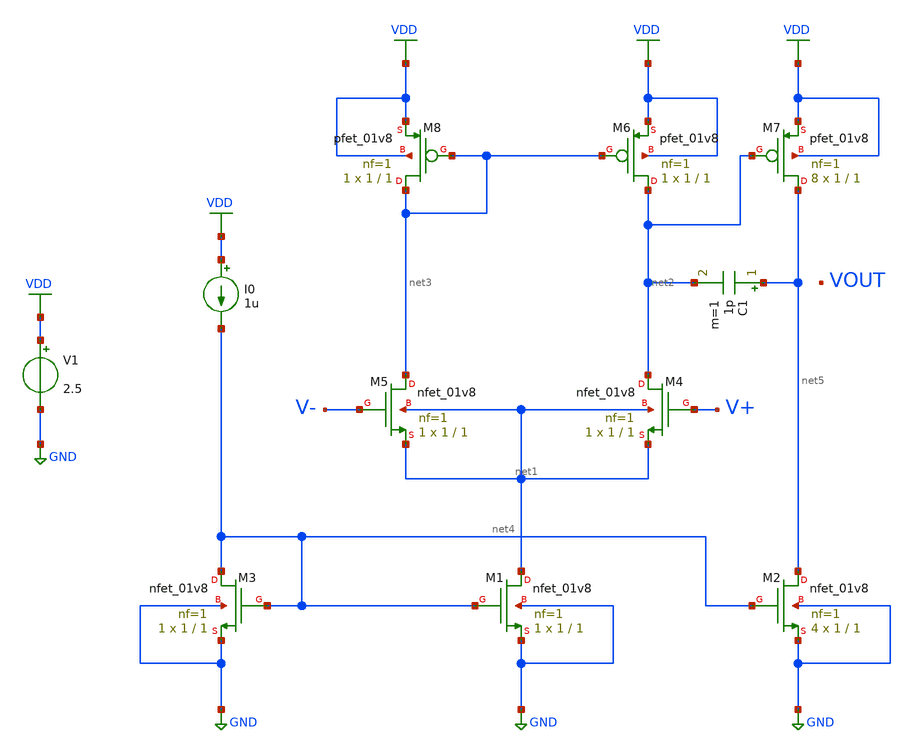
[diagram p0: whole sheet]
** sch_path: XSCHEM_SCHEMATICS/TEST_OPAMP_1/OPAMP_01.sch
**.subckt OPAMP_01
XM1 net1 net4 GND GND sky130_fd_pr__nfet_01v8 L=1 W=1 nf=1 ad='int((nf+1)/2) * W/nf * 0.29' as='int((nf+2)/2) * W/nf * 0.29'
+ pd='2*int((nf+1)/2) * (W/nf + 0.29)' ps='2*int((nf+2)/2) * (W/nf + 0.29)' nrd='0.29 / W' nrs='0.29 / W'
+ sa=0 sb=0 sd=0 mult=1 m=1
XM2 net5 net4 GND GND sky130_fd_pr__nfet_01v8 L=1 W=1 nf=1 ad='int((nf+1)/2) * W/nf * 0.29' as='int((nf+2)/2) * W/nf * 0.29'
+ pd='2*int((nf+1)/2) * (W/nf + 0.29)' ps='2*int((nf+2)/2) * (W/nf + 0.29)' nrd='0.29 / W' nrs='0.29 / W'
+ sa=0 sb=0 sd=0 mult=4 m=4
XM3 net4 net4 GND GND sky130_fd_pr__nfet_01v8 L=1 W=1 nf=1 ad='int((nf+1)/2) * W/nf * 0.29' as='int((nf+2)/2) * W/nf * 0.29'
+ pd='2*int((nf+1)/2) * (W/nf + 0.29)' ps='2*int((nf+2)/2) * (W/nf + 0.29)' nrd='0.29 / W' nrs='0.29 / W'
+ sa=0 sb=0 sd=0 mult=1 m=1
XM4 net2 V+ net1 net1 sky130_fd_pr__nfet_01v8 L=1 W=1 nf=1 ad='int((nf+1)/2) * W/nf * 0.29' as='int((nf+2)/2) * W/nf * 0.29'
+ pd='2*int((nf+1)/2) * (W/nf + 0.29)' ps='2*int((nf+2)/2) * (W/nf + 0.29)' nrd='0.29 / W' nrs='0.29 / W'
+ sa=0 sb=0 sd=0 mult=1 m=1
XM5 net3 V- net1 net1 sky130_fd_pr__nfet_01v8 L=1 W=1 nf=1 ad='int((nf+1)/2) * W/nf * 0.29' as='int((nf+2)/2) * W/nf * 0.29'
+ pd='2*int((nf+1)/2) * (W/nf + 0.29)' ps='2*int((nf+2)/2) * (W/nf + 0.29)' nrd='0.29 / W' nrs='0.29 / W'
+ sa=0 sb=0 sd=0 mult=1 m=1
XM7 net5 net2 VDD VDD sky130_fd_pr__pfet_01v8 L=1 W=1 nf=1 ad='int((nf+1)/2) * W/nf * 0.29' as='int((nf+2)/2) * W/nf * 0.29'
+ pd='2*int((nf+1)/2) * (W/nf + 0.29)' ps='2*int((nf+2)/2) * (W/nf + 0.29)' nrd='0.29 / W' nrs='0.29 / W'
+ sa=0 sb=0 sd=0 mult=8 m=8
XM6 net2 net3 VDD VDD sky130_fd_pr__pfet_01v8 L=1 W=1 nf=1 ad='int((nf+1)/2) * W/nf * 0.29' as='int((nf+2)/2) * W/nf * 0.29'
+ pd='2*int((nf+1)/2) * (W/nf + 0.29)' ps='2*int((nf+2)/2) * (W/nf + 0.29)' nrd='0.29 / W' nrs='0.29 / W'
+ sa=0 sb=0 sd=0 mult=1 m=1
XM8 net3 net3 VDD VDD sky130_fd_pr__pfet_01v8 L=1 W=1 nf=1 ad='int((nf+1)/2) * W/nf * 0.29' as='int((nf+2)/2) * W/nf * 0.29'
+ pd='2*int((nf+1)/2) * (W/nf + 0.29)' ps='2*int((nf+2)/2) * (W/nf + 0.29)' nrd='0.29 / W' nrs='0.29 / W'
+ sa=0 sb=0 sd=0 mult=1 m=1
C1 net5 net2 1p m=1
V1 VDD GND 2.5
I0 VDD net4 1u
**.ends
.GLOBAL GND
.GLOBAL VDD
.end
